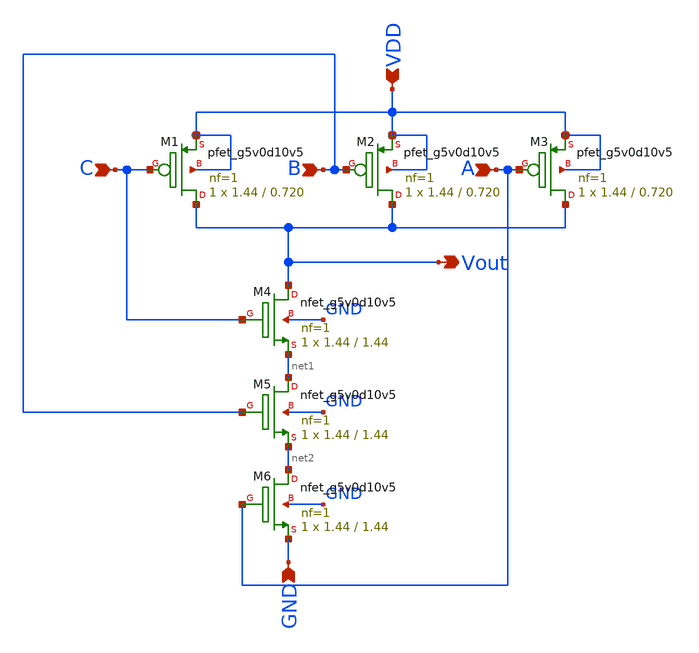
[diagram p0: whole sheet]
** sch_path: xschem/schematic_lvs/3-input-nand.sch
**.subckt 3-input-nand A B Vout C VDD GND
*.ipin A
*.ipin B
*.opin Vout
*.ipin C
*.ipin VDD
*.ipin GND
XM1 Vout C VDD VDD sky130_fd_pr__pfet_g5v0d10v5 L=0.720 W=1.44 nf=1 ad='int((1 + 1)/2) * 1.44 / 1 * 0.29'
+ as='int((1 + 2)/2) * 1.44 / 1 * 0.29' pd='2*int((1 + 1)/2) * (1.44 / 1 + 0.29)' ps='2*int((1 + 2)/2) * (1.44 / 1 + 0.29)'
+ nrd='0.29 / 1.44 ' nrs='0.29 / 1.44 ' sa=0 sb=0 sd=0 mult=1 m=1
XM2 Vout B VDD VDD sky130_fd_pr__pfet_g5v0d10v5 L=0.720 W=1.44 nf=1 ad='int((1 + 1)/2) * 1.44 / 1 * 0.29'
+ as='int((1 + 2)/2) * 1.44 / 1 * 0.29' pd='2*int((1 + 1)/2) * (1.44 / 1 + 0.29)' ps='2*int((1 + 2)/2) * (1.44 / 1 + 0.29)'
+ nrd='0.29 / 1.44 ' nrs='0.29 / 1.44 ' sa=0 sb=0 sd=0 mult=1 m=1
XM3 Vout A VDD VDD sky130_fd_pr__pfet_g5v0d10v5 L=0.720 W=1.44 nf=1 ad='int((1 + 1)/2) * 1.44 / 1 * 0.29'
+ as='int((1 + 2)/2) * 1.44 / 1 * 0.29' pd='2*int((1 + 1)/2) * (1.44 / 1 + 0.29)' ps='2*int((1 + 2)/2) * (1.44 / 1 + 0.29)'
+ nrd='0.29 / 1.44 ' nrs='0.29 / 1.44 ' sa=0 sb=0 sd=0 mult=1 m=1
XM4 Vout C net1 GND sky130_fd_pr__nfet_g5v0d10v5 L=1.44 W=1.44 nf=1 ad='int((1 + 1)/2) * 1.44 / 1 * 0.29'
+ as='int((1 + 2)/2) * 1.44 / 1 * 0.29' pd='2*int((1 + 1)/2) * (1.44 / 1 + 0.29)' ps='2*int((1 + 2)/2) * (1.44 / 1 + 0.29)'
+ nrd='0.29 / 1.44 ' nrs='0.29 / 1.44 ' sa=0 sb=0 sd=0 mult=1 m=1
XM5 net1 B net2 GND sky130_fd_pr__nfet_g5v0d10v5 L=1.44 W=1.44 nf=1 ad='int((1 + 1)/2) * 1.44 / 1 * 0.29'
+ as='int((1 + 2)/2) * 1.44 / 1 * 0.29' pd='2*int((1 + 1)/2) * (1.44 / 1 + 0.29)' ps='2*int((1 + 2)/2) * (1.44 / 1 + 0.29)'
+ nrd='0.29 / 1.44 ' nrs='0.29 / 1.44 ' sa=0 sb=0 sd=0 mult=1 m=1
XM6 net2 A GND GND sky130_fd_pr__nfet_g5v0d10v5 L=1.44 W=1.44 nf=1 ad='int((1 + 1)/2) * 1.44 / 1 * 0.29'
+ as='int((1 + 2)/2) * 1.44 / 1 * 0.29' pd='2*int((1 + 1)/2) * (1.44 / 1 + 0.29)' ps='2*int((1 + 2)/2) * (1.44 / 1 + 0.29)'
+ nrd='0.29 / 1.44 ' nrs='0.29 / 1.44 ' sa=0 sb=0 sd=0 mult=1 m=1
**.ends
.end
